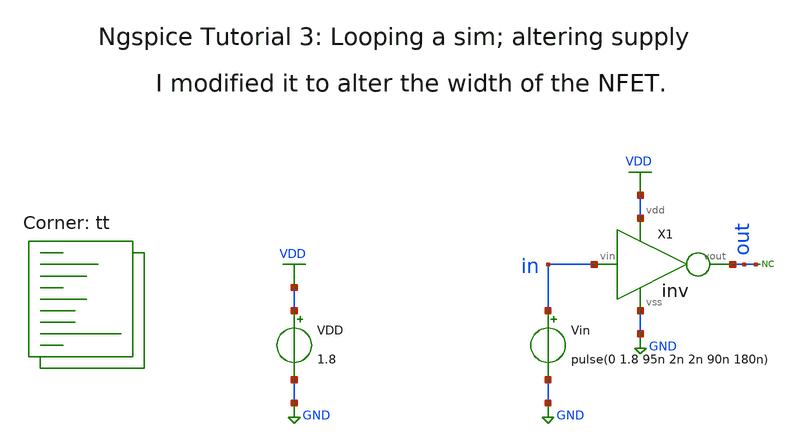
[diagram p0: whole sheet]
** sch_path: xsch/tut/ngspice_tut3.sch
**.subckt ngspice_tut3
Vin in GND pulse(0 1.8 95n 2n 2n 90n 180n)
VDD VDD GND 1.8
X1 in out VDD GND inv
* noconn out
**** begin user architecture code



* control language script

.control
let vddd = 1.0									; create a vector vddd and assign a value of 1.2
let width_mn = 1;
repeat 5									; loop start
	;alter VDD $&vddd								; alter the voltage VDD using vector vddd
	;alter @m.x1.xmn.msky130_fd_pr__nfet_01v8[W] = $&width_mn;

	alter m.x1.xmn.msky130_fd_pr__nfet_01v8 w = $&width_mn								;

	dc Vin 0 1.8 0.01								; run the dc simulation
	let vddd = vddd + 0.2								; calculate new voltage value of Vdd by updating vector vddd
	let width_mn = width_mn + 1;
end									; loop end, jump back to loop start

set xbrushwidth=2
plot dc1.v(out) dc2.v(out) dc3.v(out) dc4.v(out) dc5.v(out) dc1.v(in)
set nounits

plot deriv(dc1.v(out)) deriv(dc2.v(out)) deriv(dc3.v(out)) deriv(dc4.v(out)) deriv(dc5.v(out)) ylabel
+ 'Inverter gain V/V' xlabel 'vsweep V'
unset nounits

.endc

.end



.lib $::SKYWATER_MODELS/sky130.lib.spice tt
**** end user architecture code
**.ends
.GLOBAL VDD
.GLOBAL GND
.end
